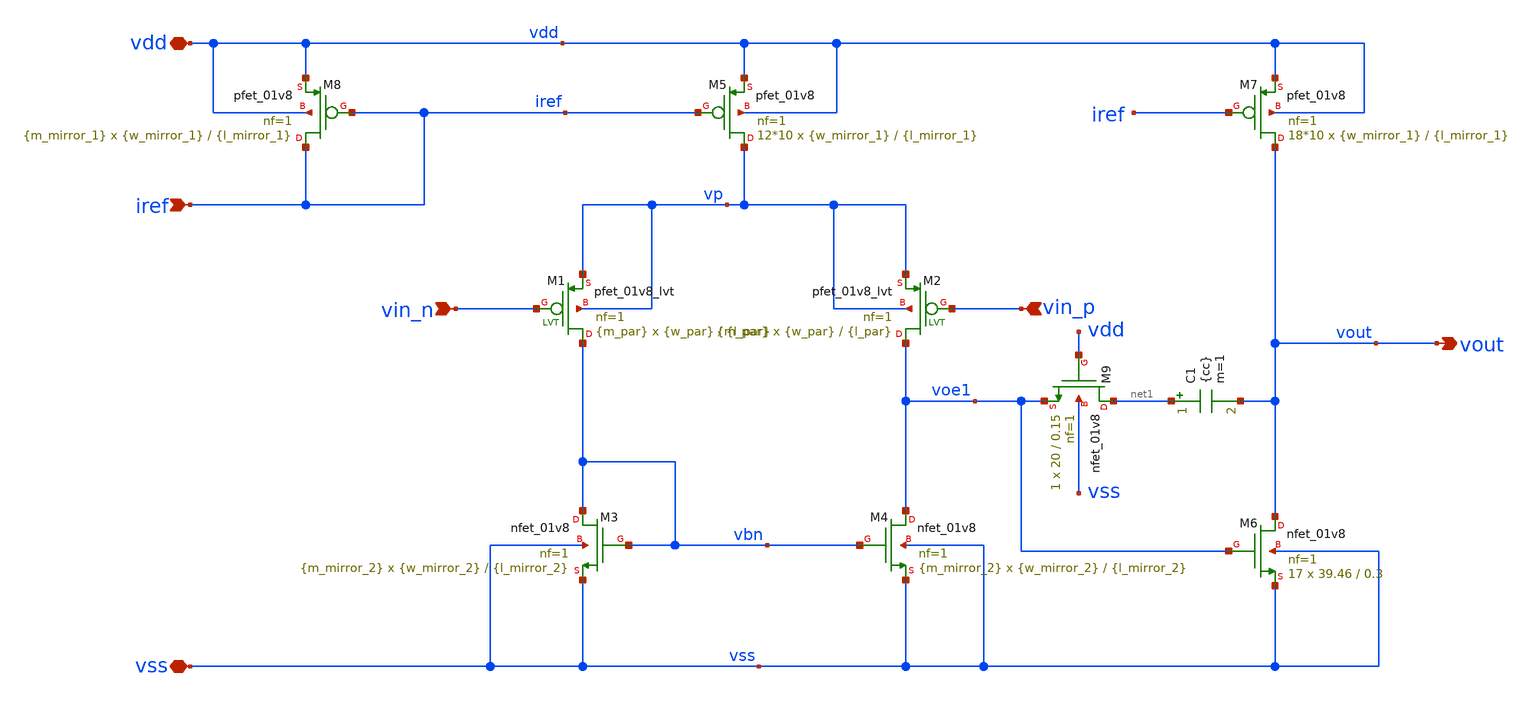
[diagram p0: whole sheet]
** sch_path: opamp.sch
**.subckt opamp vdd vss vin_n vin_p iref vout
*.iopin vdd
*.iopin vss
*.ipin vin_n
*.ipin vin_p
*.ipin iref
*.opin vout
XM3 vbn vbn vss vss sky130_fd_pr__nfet_01v8 L={l_mirror_2} W={w_mirror_2} nf=1 ad='W * 0.29' as='W * 0.29'
+ pd='2 * (W + 0.29)' ps='2 * (W + 0.29)' nrd='0.29 / W' nrs='0.29 / W' sa=0 sb=0 sd=0 mult={m_mirror_2}
+ m={m_mirror_2}
XM4 voe1 vbn vss vss sky130_fd_pr__nfet_01v8 L={l_mirror_2} W={w_mirror_2} nf=1 ad='W * 0.29' as='W * 0.29'
+ pd='2 * (W + 0.29)' ps='2 * (W + 0.29)' nrd='0.29 / W' nrs='0.29 / W' sa=0 sb=0 sd=0 mult={m_mirror_2}
+ m={m_mirror_2}
XM5 vp iref vdd vdd sky130_fd_pr__pfet_01v8 L={l_mirror_1} W={w_mirror_1} nf=1 ad='W * 0.29' as='W * 0.29'
+ pd='2 * (W + 0.29)' ps='2 * (W + 0.29)' nrd='0.29 / W' nrs='0.29 / W' sa=0 sb=0 sd=0 mult=12*10 m=12*10
XM7 vout iref vdd vdd sky130_fd_pr__pfet_01v8 L={l_mirror_1} W={w_mirror_1} nf=1 ad='W * 0.29' as='W * 0.29'
+ pd='2 * (W + 0.29)' ps='2 * (W + 0.29)' nrd='0.29 / W' nrs='0.29 / W' sa=0 sb=0 sd=0 mult=18*10 m=18*10
XM8 iref iref vdd vdd sky130_fd_pr__pfet_01v8 L={l_mirror_1} W={w_mirror_1} nf=1 ad='W * 0.29' as='W * 0.29'
+ pd='2 * (W + 0.29)' ps='2 * (W + 0.29)' nrd='0.29 / W' nrs='0.29 / W' sa=0 sb=0 sd=0 mult={m_mirror_1}
+ m={m_mirror_1}
XM9 net1 vdd voe1 vss sky130_fd_pr__nfet_01v8 L=0.15 W=20 nf=1 ad='W * 0.29' as='W * 0.29' pd='2 * (W + 0.29)'
+ ps='2 * (W + 0.29)' nrd='0.29 / W' nrs='0.29 / W' sa=0 sb=0 sd=0 mult=1 m=1
XM6 vout voe1 vss vss sky130_fd_pr__nfet_01v8 L=0.3 W=39.46 nf=1 ad='W * 0.29' as='W * 0.29' pd='2 * (W + 0.29)'
+ ps='2 * (W + 0.29)' nrd='0.29 / W' nrs='0.29 / W' sa=0 sb=0 sd=0 mult=17 m=17
XM1 vbn vin_n vp vp sky130_fd_pr__pfet_01v8_lvt L={l_par} W={w_par} nf=1 ad='int((nf+1)/2) * W/nf * 0.29'
+ as='int((nf+2)/2) * W/nf * 0.29' pd='2*int((nf+1)/2) * (W/nf + 0.29)' ps='2*int((nf+2)/2) * (W/nf + 0.29)'
+ nrd='0.29 / W' nrs='0.29 / W' sa=0 sb=0 sd=0 mult={m_par} m={m_par}
XM2 voe1 vin_p vp vp sky130_fd_pr__pfet_01v8_lvt L={l_par} W={w_par} nf=1 ad='int((nf+1)/2) * W/nf * 0.29'
+ as='int((nf+2)/2) * W/nf * 0.29' pd='2*int((nf+1)/2) * (W/nf + 0.29)' ps='2*int((nf+2)/2) * (W/nf + 0.29)'
+ nrd='0.29 / W' nrs='0.29 / W' sa=0 sb=0 sd=0 mult={m_par} m={m_par}
C1 net1 vout {cc} m=1
**.ends
.end
